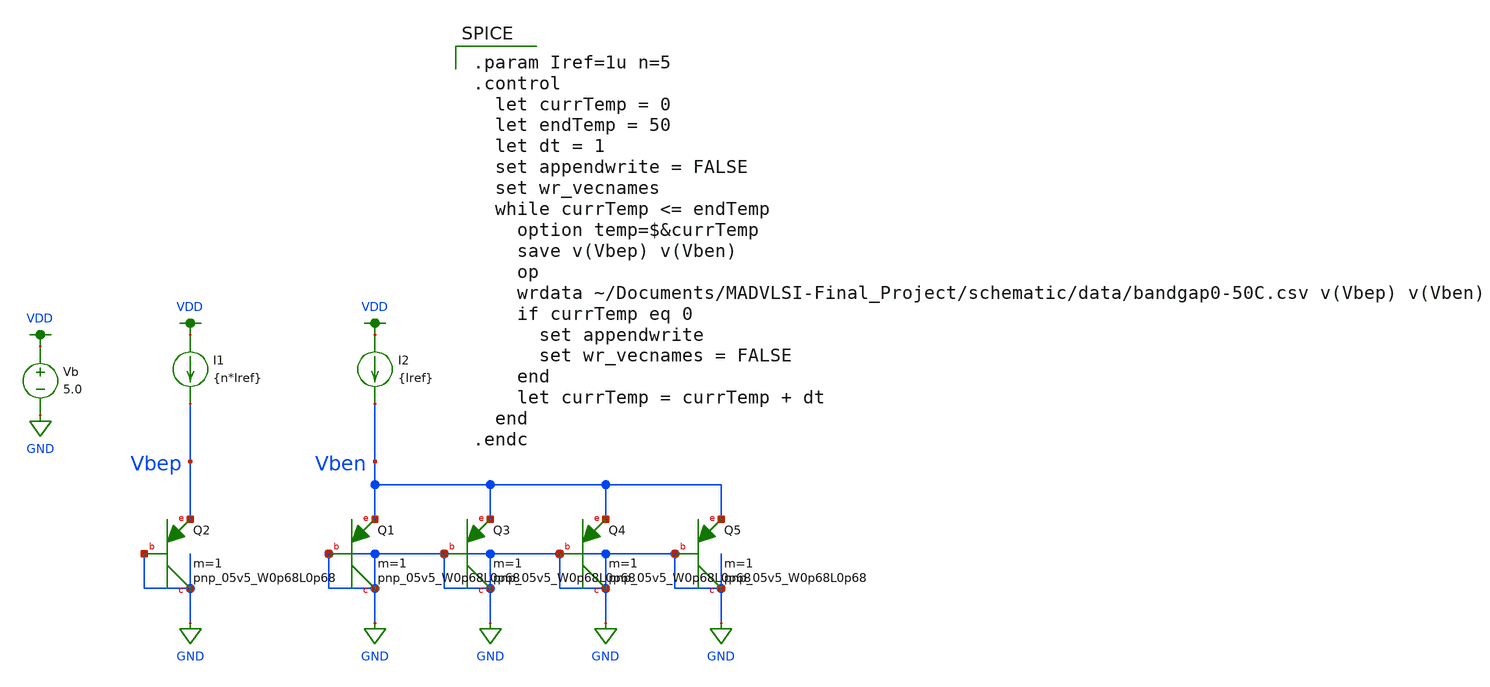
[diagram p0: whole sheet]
** sch_path: schematic/test/Vtemp_test.sch
**.subckt Vtemp_test
XQ2 GND GND Vbep sky130_fd_pr__pnp_05v5_W0p68L0p68 m=1
XQ1 GND GND Vben sky130_fd_pr__pnp_05v5_W0p68L0p68 m=1
XQ3 GND GND Vben sky130_fd_pr__pnp_05v5_W0p68L0p68 m=1
XQ4 GND GND Vben sky130_fd_pr__pnp_05v5_W0p68L0p68 m=1
XQ5 GND GND Vben sky130_fd_pr__pnp_05v5_W0p68L0p68 m=1
I1 VDD Vbep {n*Iref}
I2 VDD Vben {Iref}
Vb VDD GND 5.0
**** begin user architecture code

.option wnflag=1
.param MC_SWITCH=0.0
.lib ~/skywater/skywater-pdk/libraries/sky130_fd_pr_ngspice/latest/models/sky130.lib.spice tt


.param Iref=1u n=5
.control
  let currTemp = 0
  let endTemp = 50
  let dt = 1
  set appendwrite = FALSE
  set wr_vecnames
  while currTemp <= endTemp
    option temp=$&currTemp
    save v(Vbep) v(Vben)
    op
    wrdata ~/Documents/MADVLSI-Final_Project/schematic/data/bandgap0-50C.csv v(Vbep) v(Vben)
    if currTemp eq 0
      set appendwrite
      set wr_vecnames = FALSE
    end
    let currTemp = currTemp + dt
  end
.endc

**** end user architecture code
**.ends
.GLOBAL GND
.GLOBAL VDD
.end
